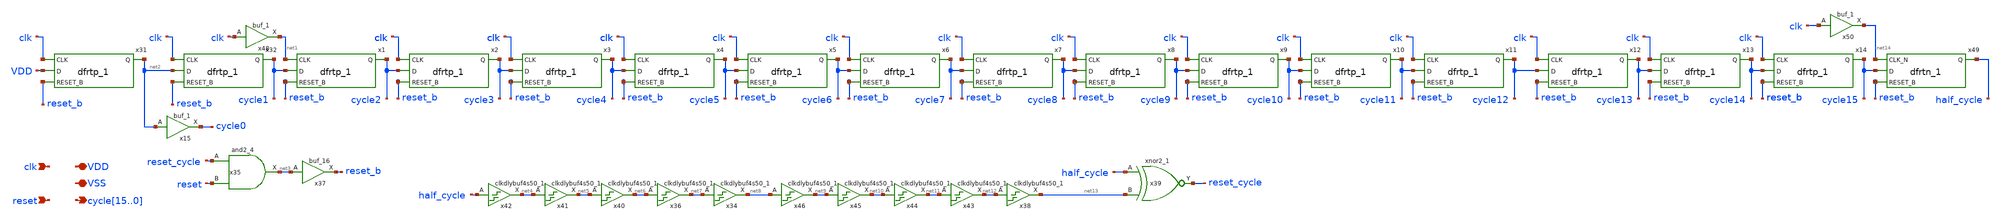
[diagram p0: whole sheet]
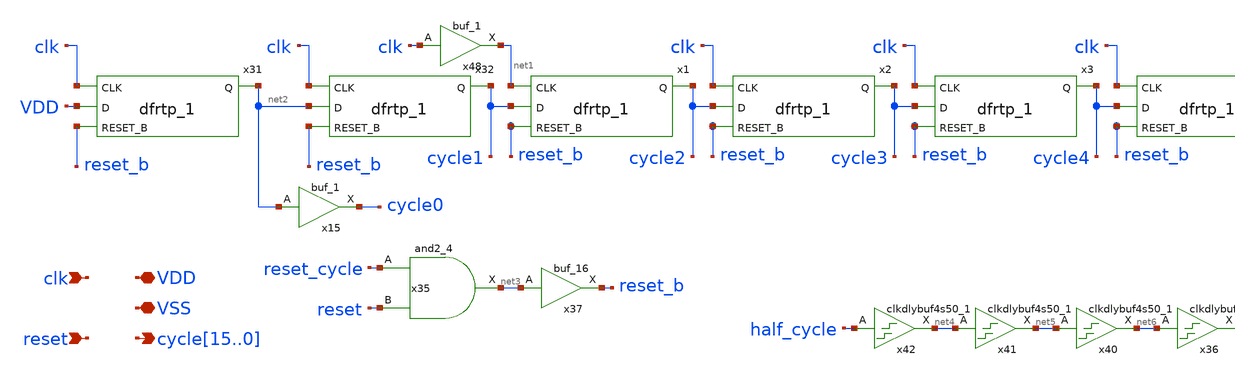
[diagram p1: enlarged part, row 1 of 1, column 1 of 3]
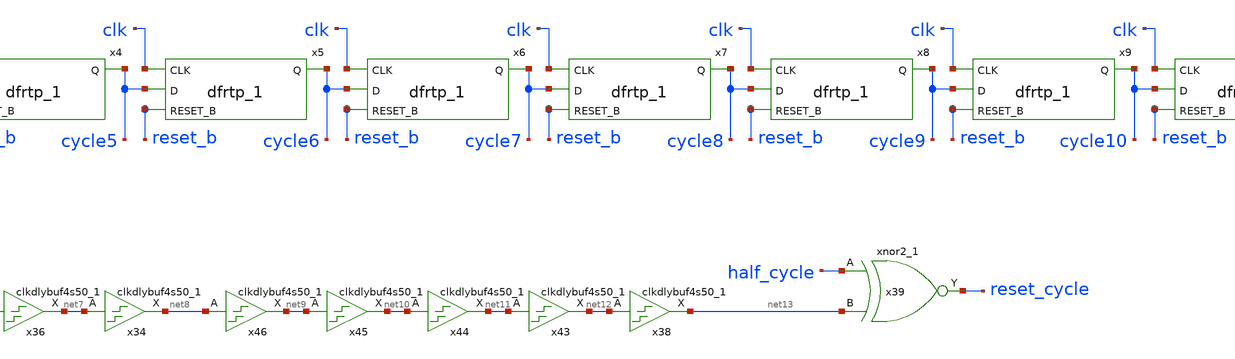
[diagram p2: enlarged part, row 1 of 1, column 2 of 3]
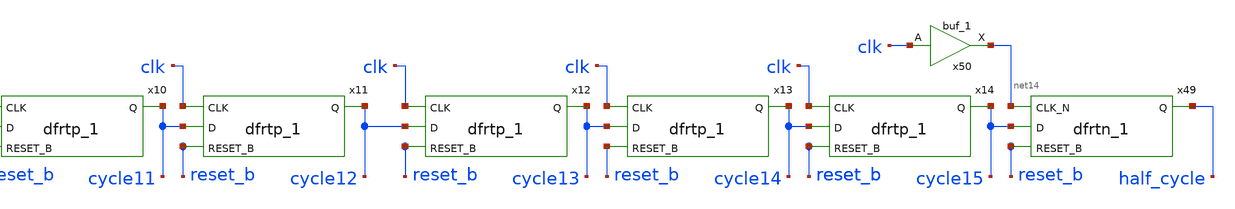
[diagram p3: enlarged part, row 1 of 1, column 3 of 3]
** sch_path: xschem/src/shifted_clock_generator/shifted_clock_generator.sch
**.subckt shifted_clock_generator
*+ cycle15,cycle14,cycle13,cycle12,cycle11,cycle10,cycle9,cycle8,cycle7,cycle6,cycle5,cycle4,cycle3,cycle2,cycle1,cycle0 VSS VDD clk reset
*.opin
*+ cycle15,cycle14,cycle13,cycle12,cycle11,cycle10,cycle9,cycle8,cycle7,cycle6,cycle5,cycle4,cycle3,cycle2,cycle1,cycle0
*.iopin VSS
*.iopin VDD
*.ipin clk
*.ipin reset
x32 clk net2 reset_b VSS VSS VDD VDD cycle1 sky130_fd_sc_hd__dfrtp_1
x1 net1 cycle1 reset_b VSS VSS VDD VDD cycle2 sky130_fd_sc_hd__dfrtp_1
x2 clk cycle2 reset_b VSS VSS VDD VDD cycle3 sky130_fd_sc_hd__dfrtp_1
x3 clk cycle3 reset_b VSS VSS VDD VDD cycle4 sky130_fd_sc_hd__dfrtp_1
x4 clk cycle4 reset_b VSS VSS VDD VDD cycle5 sky130_fd_sc_hd__dfrtp_1
x5 clk cycle5 reset_b VSS VSS VDD VDD cycle6 sky130_fd_sc_hd__dfrtp_1
x6 clk cycle6 reset_b VSS VSS VDD VDD cycle7 sky130_fd_sc_hd__dfrtp_1
x7 clk cycle7 reset_b VSS VSS VDD VDD cycle8 sky130_fd_sc_hd__dfrtp_1
x8 clk cycle8 reset_b VSS VSS VDD VDD cycle9 sky130_fd_sc_hd__dfrtp_1
x9 clk cycle9 reset_b VSS VSS VDD VDD cycle10 sky130_fd_sc_hd__dfrtp_1
x10 clk cycle10 reset_b VSS VSS VDD VDD cycle11 sky130_fd_sc_hd__dfrtp_1
x11 clk cycle11 reset_b VSS VSS VDD VDD cycle12 sky130_fd_sc_hd__dfrtp_1
x12 clk cycle12 reset_b VSS VSS VDD VDD cycle13 sky130_fd_sc_hd__dfrtp_1
x13 clk cycle13 reset_b VSS VSS VDD VDD cycle14 sky130_fd_sc_hd__dfrtp_1
x14 clk cycle14 reset_b VSS VSS VDD VDD cycle15 sky130_fd_sc_hd__dfrtp_1
x31 clk VDD reset_b VSS VSS VDD VDD net2 sky130_fd_sc_hd__dfrtp_1
x37 net3 VSS VSS VDD VDD reset_b sky130_fd_sc_hd__buf_16
x35 reset_cycle reset VSS VSS VDD VDD net3 sky130_fd_sc_hd__and2_4
x34 net7 VSS VSS VDD VDD net8 sky130_fd_sc_hd__clkdlybuf4s50_1
x39 half_cycle net13 VSS VSS VDD VDD reset_cycle sky130_fd_sc_hd__xnor2_1
x36 net6 VSS VSS VDD VDD net7 sky130_fd_sc_hd__clkdlybuf4s50_1
x40 net5 VSS VSS VDD VDD net6 sky130_fd_sc_hd__clkdlybuf4s50_1
x41 net4 VSS VSS VDD VDD net5 sky130_fd_sc_hd__clkdlybuf4s50_1
x42 half_cycle VSS VSS VDD VDD net4 sky130_fd_sc_hd__clkdlybuf4s50_1
x38 net12 VSS VSS VDD VDD net13 sky130_fd_sc_hd__clkdlybuf4s50_1
x43 net11 VSS VSS VDD VDD net12 sky130_fd_sc_hd__clkdlybuf4s50_1
x44 net10 VSS VSS VDD VDD net11 sky130_fd_sc_hd__clkdlybuf4s50_1
x45 net9 VSS VSS VDD VDD net10 sky130_fd_sc_hd__clkdlybuf4s50_1
x46 net8 VSS VSS VDD VDD net9 sky130_fd_sc_hd__clkdlybuf4s50_1
x48 clk VSS VSS VDD VDD net1 sky130_fd_sc_hd__buf_1
x49 net14 cycle15 reset_b VSS VSS VDD VDD half_cycle sky130_fd_sc_hd__dfrtn_1
x50 clk VSS VSS VDD VDD net14 sky130_fd_sc_hd__buf_1
x15 net2 VSS VSS VDD VDD cycle0 sky130_fd_sc_hd__buf_1
**.ends
.end
